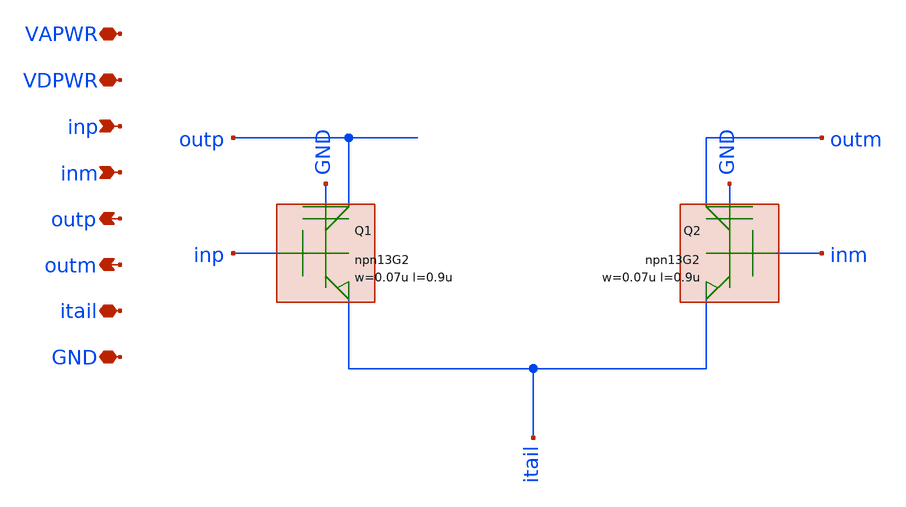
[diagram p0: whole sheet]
** sch_path: xschem/diff_npn.sch
**.subckt diff_npn VAPWR VDPWR inp inm outp outm itail GND
*.iopin VAPWR
*.iopin VDPWR
*.ipin inp
*.ipin inm
*.opin outp
*.opin outm
*.iopin itail
*.iopin GND
KQ1 npn13G2 w=0.07u l=0.9u nx=1 ny=1
KQ2 npn13G2 w=0.07u l=0.9u nx=1 ny=1
**.ends
.end
